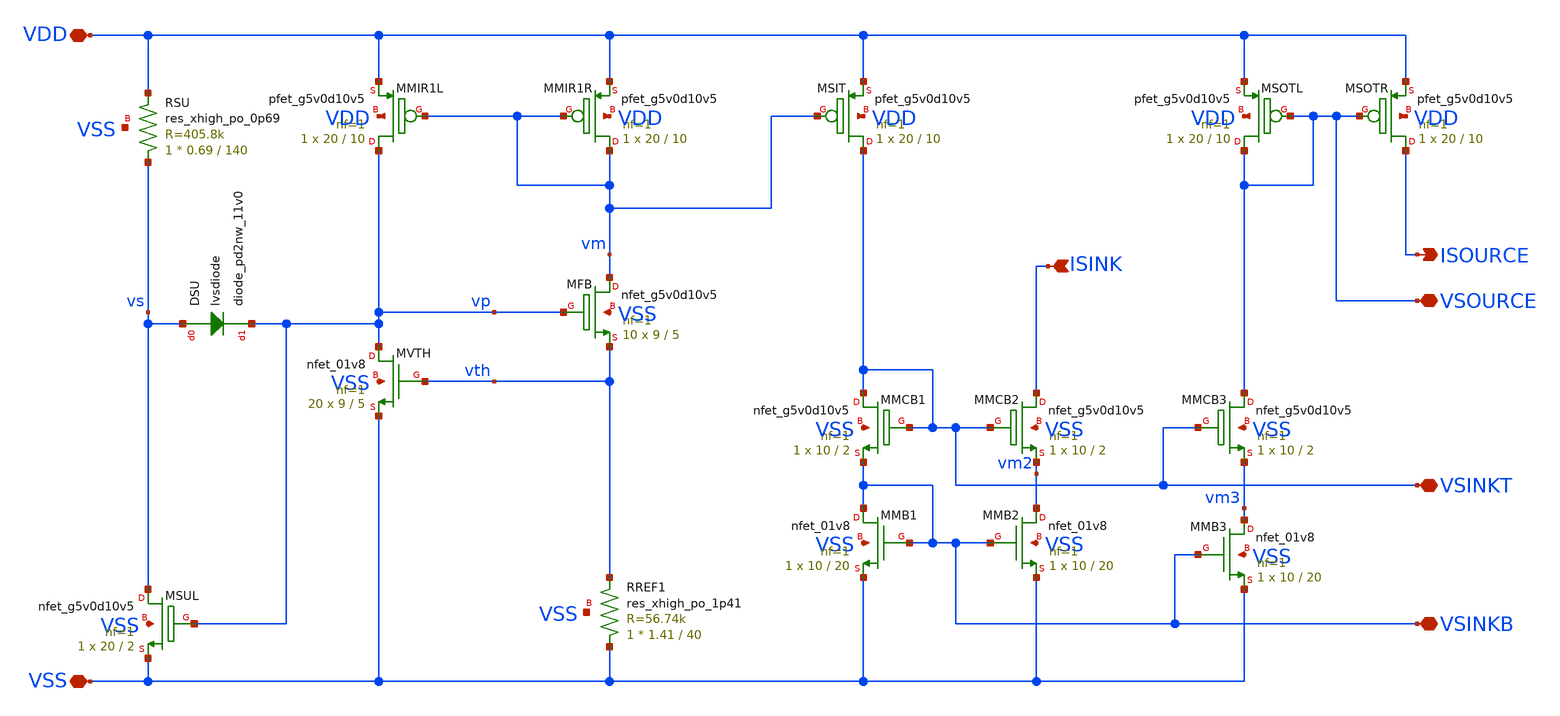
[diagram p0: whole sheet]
** sch_path: tt08/ip/vthref_tt/xschem/vthref.sch
**.subckt vthref VSS VDD ISINK ISOURCE VSOURCE VSINKT VSINKB
*.iopin VSS
*.iopin VDD
*.ipin ISINK
*.opin ISOURCE
*.iopin VSOURCE
*.iopin VSINKT
*.iopin VSINKB
XMFB vm vp vth VSS sky130_fd_pr__nfet_g5v0d10v5 L=5 W=9 nf=1 ad='int((nf+1)/2) * W/nf * 0.29' as='int((nf+2)/2) * W/nf * 0.29'
+ pd='2*int((nf+1)/2) * (W/nf + 0.29)' ps='2*int((nf+2)/2) * (W/nf + 0.29)' nrd='0.29 / W' nrs='0.29 / W'
+ sa=0 sb=0 sd=0 mult=10 m=10
XMMCB1 VSINKT VSINKT VSINKB VSS sky130_fd_pr__nfet_g5v0d10v5 L=2 W=10 nf=1 ad='int((nf+1)/2) * W/nf * 0.29'
+ as='int((nf+2)/2) * W/nf * 0.29' pd='2*int((nf+1)/2) * (W/nf + 0.29)' ps='2*int((nf+2)/2) * (W/nf + 0.29)'
+ nrd='0.29 / W' nrs='0.29 / W' sa=0 sb=0 sd=0 mult=1 m=1
XMMCB2 ISINK VSINKT vm2 VSS sky130_fd_pr__nfet_g5v0d10v5 L=2 W=10 nf=1 ad='int((nf+1)/2) * W/nf * 0.29'
+ as='int((nf+2)/2) * W/nf * 0.29' pd='2*int((nf+1)/2) * (W/nf + 0.29)' ps='2*int((nf+2)/2) * (W/nf + 0.29)'
+ nrd='0.29 / W' nrs='0.29 / W' sa=0 sb=0 sd=0 mult=1 m=1
XMSOTL VSOURCE VSOURCE VDD VDD sky130_fd_pr__pfet_g5v0d10v5 L=10 W=20 nf=1 ad='int((nf+1)/2) * W/nf * 0.29'
+ as='int((nf+2)/2) * W/nf * 0.29' pd='2*int((nf+1)/2) * (W/nf + 0.29)' ps='2*int((nf+2)/2) * (W/nf + 0.29)'
+ nrd='0.29 / W' nrs='0.29 / W' sa=0 sb=0 sd=0 mult=1 m=1
XMSOTR ISOURCE VSOURCE VDD VDD sky130_fd_pr__pfet_g5v0d10v5 L=10 W=20 nf=1 ad='int((nf+1)/2) * W/nf * 0.29'
+ as='int((nf+2)/2) * W/nf * 0.29' pd='2*int((nf+1)/2) * (W/nf + 0.29)' ps='2*int((nf+2)/2) * (W/nf + 0.29)'
+ nrd='0.29 / W' nrs='0.29 / W' sa=0 sb=0 sd=0 mult=1 m=1
XMMIR1R vm vm VDD VDD sky130_fd_pr__pfet_g5v0d10v5 L=10 W=20 nf=1 ad='int((nf+1)/2) * W/nf * 0.29' as='int((nf+2)/2) * W/nf * 0.29'
+ pd='2*int((nf+1)/2) * (W/nf + 0.29)' ps='2*int((nf+2)/2) * (W/nf + 0.29)' nrd='0.29 / W' nrs='0.29 / W'
+ sa=0 sb=0 sd=0 mult=1 m=1
XMMIR1L vp vm VDD VDD sky130_fd_pr__pfet_g5v0d10v5 L=10 W=20 nf=1 ad='int((nf+1)/2) * W/nf * 0.29' as='int((nf+2)/2) * W/nf * 0.29'
+ pd='2*int((nf+1)/2) * (W/nf + 0.29)' ps='2*int((nf+2)/2) * (W/nf + 0.29)' nrd='0.29 / W' nrs='0.29 / W'
+ sa=0 sb=0 sd=0 mult=1 m=1
XMSIT VSINKT vm VDD VDD sky130_fd_pr__pfet_g5v0d10v5 L=10 W=20 nf=1 ad='int((nf+1)/2) * W/nf * 0.29'
+ as='int((nf+2)/2) * W/nf * 0.29' pd='2*int((nf+1)/2) * (W/nf + 0.29)' ps='2*int((nf+2)/2) * (W/nf + 0.29)'
+ nrd='0.29 / W' nrs='0.29 / W' sa=0 sb=0 sd=0 mult=1 m=1
XMMCB3 VSOURCE VSINKT vm3 VSS sky130_fd_pr__nfet_g5v0d10v5 L=2 W=10 nf=1 ad='int((nf+1)/2) * W/nf * 0.29'
+ as='int((nf+2)/2) * W/nf * 0.29' pd='2*int((nf+1)/2) * (W/nf + 0.29)' ps='2*int((nf+2)/2) * (W/nf + 0.29)'
+ nrd='0.29 / W' nrs='0.29 / W' sa=0 sb=0 sd=0 mult=1 m=1
XMVTH vp vth VSS VSS sky130_fd_pr__nfet_01v8 L=5 W=9 nf=1 ad='int((nf+1)/2) * W/nf * 0.29' as='int((nf+2)/2) * W/nf * 0.29'
+ pd='2*int((nf+1)/2) * (W/nf + 0.29)' ps='2*int((nf+2)/2) * (W/nf + 0.29)' nrd='0.29 / W' nrs='0.29 / W'
+ sa=0 sb=0 sd=0 mult=20 m=20
XMMB1 VSINKB VSINKB VSS VSS sky130_fd_pr__nfet_01v8 L=20 W=10 nf=1 ad='int((nf+1)/2) * W/nf * 0.29' as='int((nf+2)/2) * W/nf * 0.29'
+ pd='2*int((nf+1)/2) * (W/nf + 0.29)' ps='2*int((nf+2)/2) * (W/nf + 0.29)' nrd='0.29 / W' nrs='0.29 / W'
+ sa=0 sb=0 sd=0 mult=1 m=1
XMMB2 vm2 VSINKB VSS VSS sky130_fd_pr__nfet_01v8 L=20 W=10 nf=1 ad='int((nf+1)/2) * W/nf * 0.29' as='int((nf+2)/2) * W/nf * 0.29'
+ pd='2*int((nf+1)/2) * (W/nf + 0.29)' ps='2*int((nf+2)/2) * (W/nf + 0.29)' nrd='0.29 / W' nrs='0.29 / W'
+ sa=0 sb=0 sd=0 mult=1 m=1
XMMB3 vm3 VSINKB VSS VSS sky130_fd_pr__nfet_01v8 L=20 W=10 nf=1 ad='int((nf+1)/2) * W/nf * 0.29' as='int((nf+2)/2) * W/nf * 0.29'
+ pd='2*int((nf+1)/2) * (W/nf + 0.29)' ps='2*int((nf+2)/2) * (W/nf + 0.29)' nrd='0.29 / W' nrs='0.29 / W'
+ sa=0 sb=0 sd=0 mult=1 m=1
DSU vs vp sky130_fd_pr__diode_pd2nw_11v0 area=1e+12
XMSUL vs vp VSS VSS sky130_fd_pr__nfet_g5v0d10v5 L=2 W=20 nf=1 ad='int((nf+1)/2) * W/nf * 0.29' as='int((nf+2)/2) * W/nf * 0.29'
+ pd='2*int((nf+1)/2) * (W/nf + 0.29)' ps='2*int((nf+2)/2) * (W/nf + 0.29)' nrd='0.29 / W' nrs='0.29 / W'
+ sa=0 sb=0 sd=0 mult=1 m=1
XRSU vs VDD VSS sky130_fd_pr__res_xhigh_po_0p69 L=140 mult=1 m=1
XRREF1 VSS vth VSS sky130_fd_pr__res_xhigh_po_1p41 L=40 mult=1 m=1
**.ends
.end
